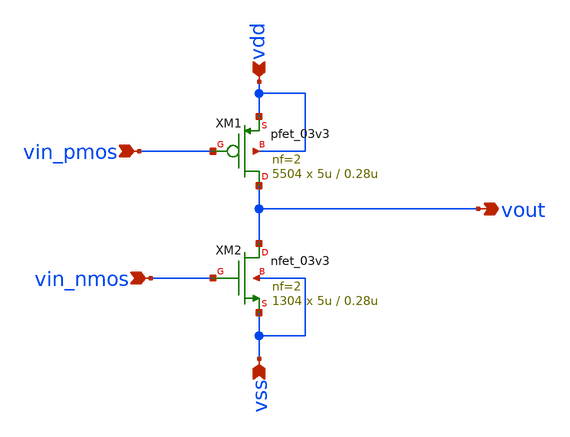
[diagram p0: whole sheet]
** sch_path: designs/libs/core_analog/Output_Stage/Output_Stage_32_ohm.sch
**.subckt Output_Stage_32_ohm vin_pmos vdd vss vout vin_nmos
*.ipin vin_pmos
*.ipin vdd
*.ipin vss
*.opin vout
*.ipin vin_nmos
XM1 vout vin_pmos vdd vdd pfet_03v3 L=0.28u W=5u nf=2 ad='int((nf+1)/2) * W/nf * 0.18u' as='int((nf+2)/2) * W/nf * 0.18u'
+ pd='2*int((nf+1)/2) * (W/nf + 0.18u)' ps='2*int((nf+2)/2) * (W/nf + 0.18u)' nrd='0.18u / W' nrs='0.18u / W'
+ sa=0 sb=0 sd=0 m=5504
XM2 vout vin_nmos vss vss nfet_03v3 L=0.28u W=5u nf=2 ad='int((nf+1)/2) * W/nf * 0.18u' as='int((nf+2)/2) * W/nf * 0.18u'
+ pd='2*int((nf+1)/2) * (W/nf + 0.18u)' ps='2*int((nf+2)/2) * (W/nf + 0.18u)' nrd='0.18u / W' nrs='0.18u / W'
+ sa=0 sb=0 sd=0 m=1304
**.ends
.end
